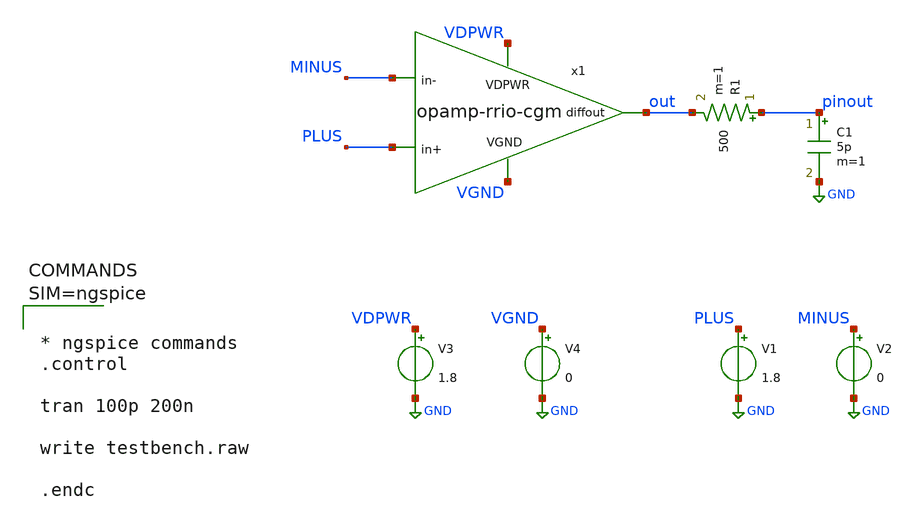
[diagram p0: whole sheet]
** sch_path: xschem/testbench.sch
**.subckt testbench
R1 pinout out 500 m=1
C1 pinout GND 5p m=1
x1 VDPWR out PLUS MINUS VGND opamp-rrio-cgm
V1 PLUS GND 1.8
V2 MINUS GND 0
V3 VDPWR GND 1.8
V4 VGND GND 0
**** begin user architecture code



* ngspice commands
.control

tran 100p 200n

write testbench.raw

.endc




** opencircuitdesign pdks install
.lib $::SKYWATER_MODELS/sky130.lib.spice tt


**** end user architecture code
**.ends

* expanding   symbol:  opamp-rrio-cgm.sym # of pins=5
** sym_path: xschem/opamp-rrio-cgm.sym
** sch_path: xschem/opamp-rrio-cgm.sch
.subckt opamp-rrio-cgm VDPWR diffout in+ in- VGND
*.ipin in+
*.ipin in-
*.opin diffout
*.ipin VDPWR
*.ipin VGND
XM1 net2 in+ net4 VGND sky130_fd_pr__nfet_01v8_lvt L=0.5 W=80 nf=4 ad='int((nf+1)/2) * W/nf * 0.29' as='int((nf+2)/2) * W/nf * 0.29'
+ pd='2*int((nf+1)/2) * (W/nf + 0.29)' ps='2*int((nf+2)/2) * (W/nf + 0.29)' nrd='0.29 / W' nrs='0.29 / W'
+ sa=0 sb=0 sd=0 mult=1 m=1
XM2 net6 in+ net1 VDPWR sky130_fd_pr__pfet_01v8_lvt L=0.5 W=200 nf=6 ad='int((nf+1)/2) * W/nf * 0.29'
+ as='int((nf+2)/2) * W/nf * 0.29' pd='2*int((nf+1)/2) * (W/nf + 0.29)' ps='2*int((nf+2)/2) * (W/nf + 0.29)'
+ nrd='0.29 / W' nrs='0.29 / W' sa=0 sb=0 sd=0 mult=1 m=1
XM3 net3 in- net4 VGND sky130_fd_pr__nfet_01v8_lvt L=0.5 W=80 nf=4 ad='int((nf+1)/2) * W/nf * 0.29' as='int((nf+2)/2) * W/nf * 0.29'
+ pd='2*int((nf+1)/2) * (W/nf + 0.29)' ps='2*int((nf+2)/2) * (W/nf + 0.29)' nrd='0.29 / W' nrs='0.29 / W'
+ sa=0 sb=0 sd=0 mult=1 m=1
XM4 net5 in- net1 VDPWR sky130_fd_pr__pfet_01v8_lvt L=0.5 W=200 nf=6 ad='int((nf+1)/2) * W/nf * 0.29'
+ as='int((nf+2)/2) * W/nf * 0.29' pd='2*int((nf+1)/2) * (W/nf + 0.29)' ps='2*int((nf+2)/2) * (W/nf + 0.29)'
+ nrd='0.29 / W' nrs='0.29 / W' sa=0 sb=0 sd=0 mult=1 m=1
XM5 net6 net18 net1 VDPWR sky130_fd_pr__pfet_01v8_lvt L=0.5 W=200 nf=6 ad='int((nf+1)/2) * W/nf * 0.29'
+ as='int((nf+2)/2) * W/nf * 0.29' pd='2*int((nf+1)/2) * (W/nf + 0.29)' ps='2*int((nf+2)/2) * (W/nf + 0.29)'
+ nrd='0.29 / W' nrs='0.29 / W' sa=0 sb=0 sd=0 mult=1 m=1
XM6 net5 net18 net1 VDPWR sky130_fd_pr__pfet_01v8_lvt L=0.5 W=200 nf=6 ad='int((nf+1)/2) * W/nf * 0.29'
+ as='int((nf+2)/2) * W/nf * 0.29' pd='2*int((nf+1)/2) * (W/nf + 0.29)' ps='2*int((nf+2)/2) * (W/nf + 0.29)'
+ nrd='0.29 / W' nrs='0.29 / W' sa=0 sb=0 sd=0 mult=1 m=1
XM7 net3 net18 net4 VGND sky130_fd_pr__nfet_01v8_lvt L=0.5 W=80 nf=1 ad='int((nf+1)/2) * W/nf * 0.29'
+ as='int((nf+2)/2) * W/nf * 0.29' pd='2*int((nf+1)/2) * (W/nf + 0.29)' ps='2*int((nf+2)/2) * (W/nf + 0.29)'
+ nrd='0.29 / W' nrs='0.29 / W' sa=0 sb=0 sd=0 mult=1 m=1
XM8 net2 net18 net4 VGND sky130_fd_pr__nfet_01v8_lvt L=0.5 W=80 nf=1 ad='int((nf+1)/2) * W/nf * 0.29'
+ as='int((nf+2)/2) * W/nf * 0.29' pd='2*int((nf+1)/2) * (W/nf + 0.29)' ps='2*int((nf+2)/2) * (W/nf + 0.29)'
+ nrd='0.29 / W' nrs='0.29 / W' sa=0 sb=0 sd=0 mult=1 m=1
XM9 net1 net7 VDPWR VDPWR sky130_fd_pr__pfet_01v8_lvt L=6 W=45 nf=1 ad='int((nf+1)/2) * W/nf * 0.29'
+ as='int((nf+2)/2) * W/nf * 0.29' pd='2*int((nf+1)/2) * (W/nf + 0.29)' ps='2*int((nf+2)/2) * (W/nf + 0.29)'
+ nrd='0.29 / W' nrs='0.29 / W' sa=0 sb=0 sd=0 mult=1 m=1
XM12 net7 net7 VDPWR VDPWR sky130_fd_pr__pfet_01v8_lvt L=1 W=30 nf=1 ad='int((nf+1)/2) * W/nf * 0.29'
+ as='int((nf+2)/2) * W/nf * 0.29' pd='2*int((nf+1)/2) * (W/nf + 0.29)' ps='2*int((nf+2)/2) * (W/nf + 0.29)'
+ nrd='0.29 / W' nrs='0.29 / W' sa=0 sb=0 sd=0 mult=1 m=1
XM13 net16 net16 net7 VDPWR sky130_fd_pr__pfet_01v8_lvt L=1 W=30 nf=1 ad='int((nf+1)/2) * W/nf * 0.29'
+ as='int((nf+2)/2) * W/nf * 0.29' pd='2*int((nf+1)/2) * (W/nf + 0.29)' ps='2*int((nf+2)/2) * (W/nf + 0.29)'
+ nrd='0.29 / W' nrs='0.29 / W' sa=0 sb=0 sd=0 mult=1 m=1
XM10 net2 net8 VDPWR VDPWR sky130_fd_pr__pfet_01v8_lvt L=6 W=45 nf=1 ad='int((nf+1)/2) * W/nf * 0.29'
+ as='int((nf+2)/2) * W/nf * 0.29' pd='2*int((nf+1)/2) * (W/nf + 0.29)' ps='2*int((nf+2)/2) * (W/nf + 0.29)'
+ nrd='0.29 / W' nrs='0.29 / W' sa=0 sb=0 sd=0 mult=1 m=1
XM11 net3 net8 VDPWR VDPWR sky130_fd_pr__pfet_01v8_lvt L=6 W=45 nf=1 ad='int((nf+1)/2) * W/nf * 0.29'
+ as='int((nf+2)/2) * W/nf * 0.29' pd='2*int((nf+1)/2) * (W/nf + 0.29)' ps='2*int((nf+2)/2) * (W/nf + 0.29)'
+ nrd='0.29 / W' nrs='0.29 / W' sa=0 sb=0 sd=0 mult=1 m=1
XM14 net8 net17 net2 VDPWR sky130_fd_pr__pfet_01v8_lvt L=0.5 W=40 nf=1 ad='int((nf+1)/2) * W/nf * 0.29'
+ as='int((nf+2)/2) * W/nf * 0.29' pd='2*int((nf+1)/2) * (W/nf + 0.29)' ps='2*int((nf+2)/2) * (W/nf + 0.29)'
+ nrd='0.29 / W' nrs='0.29 / W' sa=0 sb=0 sd=0 mult=1 m=1
XM15 net13 net17 net3 VDPWR sky130_fd_pr__pfet_01v8_lvt L=0.5 W=40 nf=1 ad='int((nf+1)/2) * W/nf * 0.29'
+ as='int((nf+2)/2) * W/nf * 0.29' pd='2*int((nf+1)/2) * (W/nf + 0.29)' ps='2*int((nf+2)/2) * (W/nf + 0.29)'
+ nrd='0.29 / W' nrs='0.29 / W' sa=0 sb=0 sd=0 mult=1 m=1
XM16 net9 net12 net8 VDPWR sky130_fd_pr__pfet_01v8_lvt L=2.5 W=10 nf=1 ad='int((nf+1)/2) * W/nf * 0.29'
+ as='int((nf+2)/2) * W/nf * 0.29' pd='2*int((nf+1)/2) * (W/nf + 0.29)' ps='2*int((nf+2)/2) * (W/nf + 0.29)'
+ nrd='0.29 / W' nrs='0.29 / W' sa=0 sb=0 sd=0 mult=1 m=1
XM17 net8 net11 net9 VGND sky130_fd_pr__nfet_01v8_lvt L=2.5 W=10 nf=1 ad='int((nf+1)/2) * W/nf * 0.29'
+ as='int((nf+2)/2) * W/nf * 0.29' pd='2*int((nf+1)/2) * (W/nf + 0.29)' ps='2*int((nf+2)/2) * (W/nf + 0.29)'
+ nrd='0.29 / W' nrs='0.29 / W' sa=0 sb=0 sd=0 mult=1 m=1
XM18 net9 net19 net6 VGND sky130_fd_pr__nfet_01v8_lvt L=0.5 W=12 nf=1 ad='int((nf+1)/2) * W/nf * 0.29'
+ as='int((nf+2)/2) * W/nf * 0.29' pd='2*int((nf+1)/2) * (W/nf + 0.29)' ps='2*int((nf+2)/2) * (W/nf + 0.29)'
+ nrd='0.29 / W' nrs='0.29 / W' sa=0 sb=0 sd=0 mult=1 m=1
XM19 net15 net19 net5 VGND sky130_fd_pr__nfet_01v8_lvt L=0.5 W=12 nf=1 ad='int((nf+1)/2) * W/nf * 0.29'
+ as='int((nf+2)/2) * W/nf * 0.29' pd='2*int((nf+1)/2) * (W/nf + 0.29)' ps='2*int((nf+2)/2) * (W/nf + 0.29)'
+ nrd='0.29 / W' nrs='0.29 / W' sa=0 sb=0 sd=0 mult=1 m=1
XM20 net6 net9 VGND VGND sky130_fd_pr__nfet_01v8_lvt L=6 W=15 nf=1 ad='int((nf+1)/2) * W/nf * 0.29' as='int((nf+2)/2) * W/nf * 0.29'
+ pd='2*int((nf+1)/2) * (W/nf + 0.29)' ps='2*int((nf+2)/2) * (W/nf + 0.29)' nrd='0.29 / W' nrs='0.29 / W'
+ sa=0 sb=0 sd=0 mult=1 m=1
XM21 net5 net9 VGND VGND sky130_fd_pr__nfet_01v8_lvt L=6 W=15 nf=1 ad='int((nf+1)/2) * W/nf * 0.29' as='int((nf+2)/2) * W/nf * 0.29'
+ pd='2*int((nf+1)/2) * (W/nf + 0.29)' ps='2*int((nf+2)/2) * (W/nf + 0.29)' nrd='0.29 / W' nrs='0.29 / W'
+ sa=0 sb=0 sd=0 mult=1 m=1
XM22 net4 net16 VGND VGND sky130_fd_pr__nfet_01v8_lvt L=6 W=15 nf=1 ad='int((nf+1)/2) * W/nf * 0.29'
+ as='int((nf+2)/2) * W/nf * 0.29' pd='2*int((nf+1)/2) * (W/nf + 0.29)' ps='2*int((nf+2)/2) * (W/nf + 0.29)'
+ nrd='0.29 / W' nrs='0.29 / W' sa=0 sb=0 sd=0 mult=1 m=1
XM23 net11 net7 VDPWR VDPWR sky130_fd_pr__pfet_01v8_lvt L=1 W=5 nf=1 ad='int((nf+1)/2) * W/nf * 0.29'
+ as='int((nf+2)/2) * W/nf * 0.29' pd='2*int((nf+1)/2) * (W/nf + 0.29)' ps='2*int((nf+2)/2) * (W/nf + 0.29)'
+ nrd='0.29 / W' nrs='0.29 / W' sa=0 sb=0 sd=0 mult=1 m=1
XM25 net11 net11 net14 VGND sky130_fd_pr__nfet_01v8_lvt L=0.18 W=40 nf=2 ad='int((nf+1)/2) * W/nf * 0.29'
+ as='int((nf+2)/2) * W/nf * 0.29' pd='2*int((nf+1)/2) * (W/nf + 0.29)' ps='2*int((nf+2)/2) * (W/nf + 0.29)'
+ nrd='0.29 / W' nrs='0.29 / W' sa=0 sb=0 sd=0 mult=1 m=1
XM26 net13 net11 net15 VGND sky130_fd_pr__nfet_01v8_lvt L=0.18 W=40 nf=2 ad='int((nf+1)/2) * W/nf * 0.29'
+ as='int((nf+2)/2) * W/nf * 0.29' pd='2*int((nf+1)/2) * (W/nf + 0.29)' ps='2*int((nf+2)/2) * (W/nf + 0.29)'
+ nrd='0.29 / W' nrs='0.29 / W' sa=0 sb=0 sd=0 mult=1 m=1
XM29 diffout net13 VDPWR VDPWR sky130_fd_pr__pfet_01v8_lvt L=0.35 W=198 nf=18 ad='int((nf+1)/2) * W/nf * 0.29'
+ as='int((nf+2)/2) * W/nf * 0.29' pd='2*int((nf+1)/2) * (W/nf + 0.29)' ps='2*int((nf+2)/2) * (W/nf + 0.29)'
+ nrd='0.29 / W' nrs='0.29 / W' sa=0 sb=0 sd=0 mult=1 m=1
XM30 net14 net14 VGND VGND sky130_fd_pr__nfet_01v8_lvt L=0.18 W=5 nf=1 ad='int((nf+1)/2) * W/nf * 0.29'
+ as='int((nf+2)/2) * W/nf * 0.29' pd='2*int((nf+1)/2) * (W/nf + 0.29)' ps='2*int((nf+2)/2) * (W/nf + 0.29)'
+ nrd='0.29 / W' nrs='0.29 / W' sa=0 sb=0 sd=0 mult=1 m=1
XM31 net12 net16 VGND VGND sky130_fd_pr__nfet_01v8_lvt L=1 W=5 nf=1 ad='int((nf+1)/2) * W/nf * 0.29'
+ as='int((nf+2)/2) * W/nf * 0.29' pd='2*int((nf+1)/2) * (W/nf + 0.29)' ps='2*int((nf+2)/2) * (W/nf + 0.29)'
+ nrd='0.29 / W' nrs='0.29 / W' sa=0 sb=0 sd=0 mult=1 m=1
XM32 net20 net15 net21 VGND sky130_fd_pr__nfet_01v8_lvt L=0.18 W=60 nf=10 ad='int((nf+1)/2) * W/nf * 0.29'
+ as='int((nf+2)/2) * W/nf * 0.29' pd='2*int((nf+1)/2) * (W/nf + 0.29)' ps='2*int((nf+2)/2) * (W/nf + 0.29)'
+ nrd='0.29 / W' nrs='0.29 / W' sa=0 sb=0 sd=0 mult=1 m=1
XM33 net16 net16 VGND VGND sky130_fd_pr__nfet_01v8_lvt L=1 W=12 nf=1 ad='int((nf+1)/2) * W/nf * 0.29'
+ as='int((nf+2)/2) * W/nf * 0.29' pd='2*int((nf+1)/2) * (W/nf + 0.29)' ps='2*int((nf+2)/2) * (W/nf + 0.29)'
+ nrd='0.29 / W' nrs='0.29 / W' sa=0 sb=0 sd=0 mult=1 m=1
XC1 diffout net3 sky130_fd_pr__cap_mim_m3_1 W=0.6 L=0.6 MF=1 m=1
XC2 diffout net5 sky130_fd_pr__cap_mim_m3_1 W=0.6 L=0.6 MF=1 m=1
XM34 net17 net17 VDPWR VDPWR sky130_fd_pr__pfet_01v8_lvt L=1 W=30 nf=1 ad='int((nf+1)/2) * W/nf * 0.29'
+ as='int((nf+2)/2) * W/nf * 0.29' pd='2*int((nf+1)/2) * (W/nf + 0.29)' ps='2*int((nf+2)/2) * (W/nf + 0.29)'
+ nrd='0.29 / W' nrs='0.29 / W' sa=0 sb=0 sd=0 mult=1 m=1
XM37 net18 net19 net19 VGND sky130_fd_pr__nfet_01v8_lvt L=1 W=12 nf=1 ad='int((nf+1)/2) * W/nf * 0.29'
+ as='int((nf+2)/2) * W/nf * 0.29' pd='2*int((nf+1)/2) * (W/nf + 0.29)' ps='2*int((nf+2)/2) * (W/nf + 0.29)'
+ nrd='0.29 / W' nrs='0.29 / W' sa=0 sb=0 sd=0 mult=1 m=1
XM39 net18 net18 net17 VDPWR sky130_fd_pr__pfet_01v8_lvt L=1 W=30 nf=1 ad='int((nf+1)/2) * W/nf * 0.29'
+ as='int((nf+2)/2) * W/nf * 0.29' pd='2*int((nf+1)/2) * (W/nf + 0.29)' ps='2*int((nf+2)/2) * (W/nf + 0.29)'
+ nrd='0.29 / W' nrs='0.29 / W' sa=0 sb=0 sd=0 mult=1 m=1
XM40 net19 VGND VGND VGND sky130_fd_pr__nfet_01v8_lvt L=1 W=12 nf=1 ad='int((nf+1)/2) * W/nf * 0.29'
+ as='int((nf+2)/2) * W/nf * 0.29' pd='2*int((nf+1)/2) * (W/nf + 0.29)' ps='2*int((nf+2)/2) * (W/nf + 0.29)'
+ nrd='0.29 / W' nrs='0.29 / W' sa=0 sb=0 sd=0 mult=1 m=1
XM24 net10 net10 VDPWR VDPWR sky130_fd_pr__pfet_01v8_lvt L=0.35 W=18 nf=18 ad='int((nf+1)/2) * W/nf * 0.29'
+ as='int((nf+2)/2) * W/nf * 0.29' pd='2*int((nf+1)/2) * (W/nf + 0.29)' ps='2*int((nf+2)/2) * (W/nf + 0.29)'
+ nrd='0.29 / W' nrs='0.29 / W' sa=0 sb=0 sd=0 mult=1 m=1
XM27 net15 net12 net13 VDPWR sky130_fd_pr__pfet_01v8_lvt L=0.35 W=100 nf=4 ad='int((nf+1)/2) * W/nf * 0.29'
+ as='int((nf+2)/2) * W/nf * 0.29' pd='2*int((nf+1)/2) * (W/nf + 0.29)' ps='2*int((nf+2)/2) * (W/nf + 0.29)'
+ nrd='0.29 / W' nrs='0.29 / W' sa=0 sb=0 sd=0 mult=1 m=1
XM35 net12 net12 net10 VDPWR sky130_fd_pr__pfet_01v8_lvt L=0.35 W=100 nf=4 ad='int((nf+1)/2) * W/nf * 0.29'
+ as='int((nf+2)/2) * W/nf * 0.29' pd='2*int((nf+1)/2) * (W/nf + 0.29)' ps='2*int((nf+2)/2) * (W/nf + 0.29)'
+ nrd='0.29 / W' nrs='0.29 / W' sa=0 sb=0 sd=0 mult=1 m=1
.ends

.GLOBAL GND
.end
